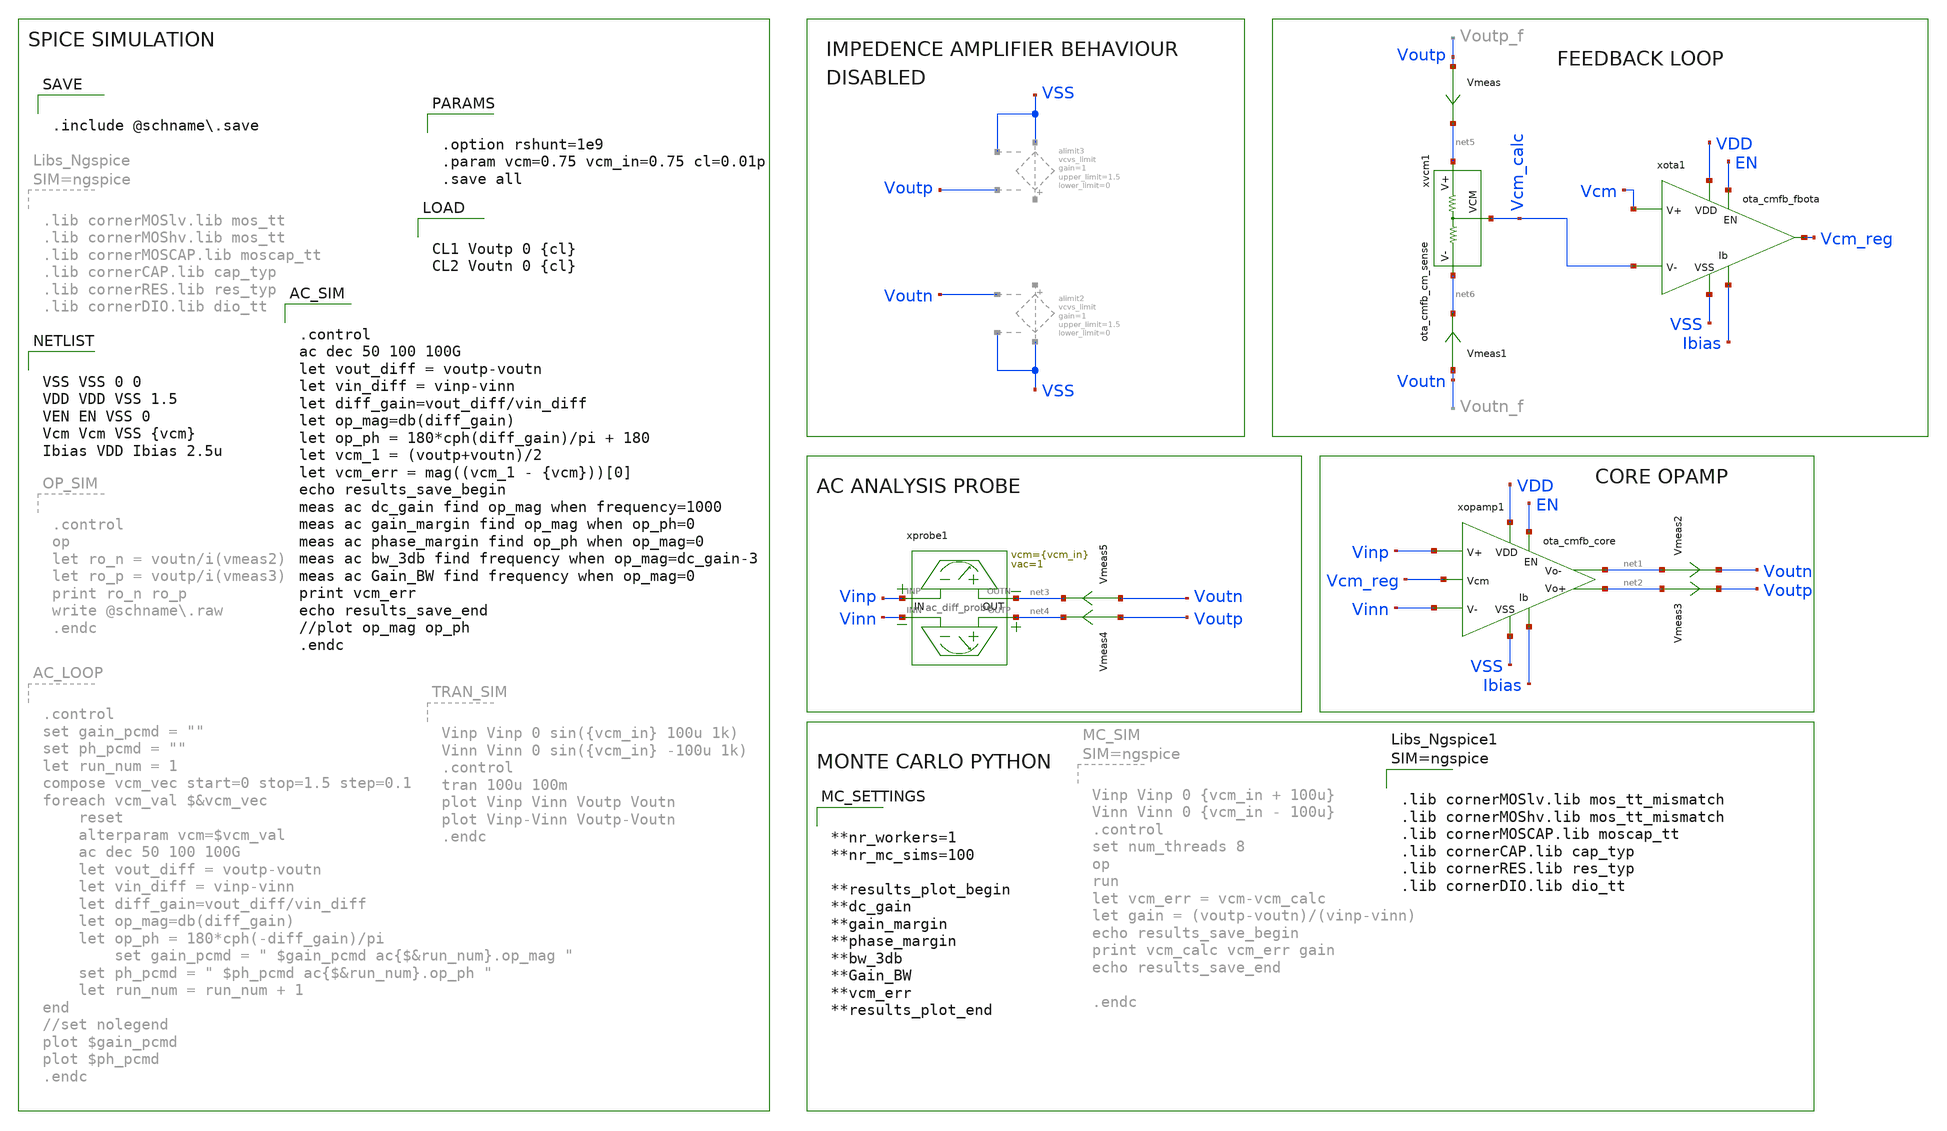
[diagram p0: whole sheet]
** sch_path: schema/ota_cmfb/ota_cmfb_tb.sch
**.subckt ota_cmfb_tb
xopamp1 VDD Vcm_reg Vinn Vinp Ibias net1 net2 VSS EN ota_cmfb_core
xprobe1 Vinp net3 Vinn net4 ac_diff_probe vcm={vcm_in} vac=1
xvcm1 net5 net6 Vcm_calc ota_cmfb_cm_sense
Vmeas Voutp net5 0
.save i(vmeas)
Vmeas1 Voutn net6 0
.save i(vmeas1)
xota1 VDD EN Ibias Vcm_calc Vcm Vcm_reg VSS ota_cmfb_fbota
Vmeas2 net1 Voutn 0
.save i(vmeas2)
Vmeas3 net2 Voutp 0
.save i(vmeas3)
Vmeas4 Voutp net4 0
.save i(vmeas4)
Vmeas5 Voutn net3 0
.save i(vmeas5)
**** begin user architecture code


VSS VSS 0 0
VDD VDD VSS 1.5
VEN EN VSS 0
Vcm Vcm VSS {vcm}
Ibias VDD Ibias 2.5u




.control
ac dec 50 100 100G
let vout_diff = voutp-voutn
let vin_diff = vinp-vinn
let diff_gain=vout_diff/vin_diff
let op_mag=db(diff_gain)
let op_ph = 180*cph(diff_gain)/pi + 180
let vcm_1 = (voutp+voutn)/2
let vcm_err = mag((vcm_1 - {vcm}))[0]
echo results_save_begin
meas ac dc_gain find op_mag when frequency=1000
meas ac gain_margin find op_mag when op_ph=0
meas ac phase_margin find op_ph when op_mag=0
meas ac bw_3db find frequency when op_mag=dc_gain-3
meas ac Gain_BW find frequency when op_mag=0
print vcm_err
echo results_save_end
//plot op_mag op_ph
.endc




.option rshunt=1e9
.param vcm=0.75 vcm_in=0.75 cl=0.01p
.save all




CL1 Voutp 0 {cl}
CL2 Voutn 0 {cl}



.include @schname.save



**nr_workers=1
**nr_mc_sims=100

**results_plot_begin
**dc_gain
**gain_margin
**phase_margin
**bw_3db
**Gain_BW
**vcm_err
**results_plot_end





.lib cornerMOSlv.lib mos_tt_mismatch
.lib cornerMOShv.lib mos_tt_mismatch
.lib cornerMOSCAP.lib moscap_tt
.lib cornerCAP.lib cap_typ
.lib cornerRES.lib res_typ
.lib cornerDIO.lib dio_tt



**** end user architecture code
**.ends

* expanding   symbol:  /foss/designs/Chipalooza2/schema/ota_cmfb_core/ota_cmfb_core.sym # of pins=9
** sym_path: schema/ota_cmfb_core/ota_cmfb_core.sym
** sch_path: schema/ota_cmfb_core/ota_cmfb_core.sch
.subckt ota_cmfb_core VDD Vcm_reg Vinn Vinp Ibias Voutn Voutp VSS EN
*.opin Voutn
*.opin Voutp
*.iopin VDD
*.iopin VSS
*.ipin Vinp
*.ipin Ibias
*.ipin Vinn
*.ipin Vcm_reg
*.ipin EN
XM1 Voutp_st1 Ibias VSS VSS sg13_lv_nmos w=0.5u l=10u ng=1 m=4 mm_ok=1
XM2 net1 Vinn Voutp_st1 VDD sg13_lv_pmos w=2.5u l=2u ng=1 m=8 mm_ok=1
XM3 Voutn_st1 Ibias VSS VSS sg13_lv_nmos w=0.5u l=10u ng=1 m=4 mm_ok=1
XM4 net1 Vinp Voutn_st1 VDD sg13_lv_pmos w=2.5u l=2u ng=1 m=8 mm_ok=1
XM5 VDD Vcm_reg net1 VDD sg13_lv_pmos w=5u l=10u ng=1 m=4 mm_ok=1
XM6 Ibias Ibias VSS VSS sg13_lv_nmos w=0.5u l=10u ng=1 m=1 mm_ok=1
XM7 Ibias EN VSS VSS sg13_lv_nmos w=0.15u l=0.13u ng=1 m=1 mm_ok=1
xsf1 VDD net2 Voutp Ibias VSS ota_cmfb_core_push_pull_output_stage
xsf2 VDD net3 Voutn Ibias VSS ota_cmfb_core_push_pull_output_stage
Vmeas Voutn_st1 net2 0
.save i(vmeas)
Vmeas1 Voutp_st1 net3 0
.save i(vmeas1)
.ends


* expanding   symbol:  /foss/designs/Chipalooza2/schema/ac_diff_probe/ac_diff_probe.sym # of pins=4
** sym_path: schema/ac_diff_probe/ac_diff_probe.sym
** sch_path: schema/ac_diff_probe/ac_diff_probe.sch
.subckt ac_diff_probe INP OUTN INN OUTP  vcm=0.75 vac=0.1
*.iopin OUTN
*.iopin INP
*.iopin OUTP
*.iopin INN
xprobe1 OUTN INP ac_probe vcm={vcm} vac={vac}
xprobe2 OUTP INN ac_probe vcm={vcm} vac=-{vac}
.ends


* expanding   symbol:  /foss/designs/Chipalooza2/schema/ota_cmfb_cm_sense/ota_cmfb_cm_sense.sym # of
*+ pins=3
** sym_path: schema/ota_cmfb_cm_sense/ota_cmfb_cm_sense.sym
** sch_path: schema/ota_cmfb_cm_sense/ota_cmfb_cm_sense.sch
.subckt ota_cmfb_cm_sense Voutp Voutn VCM
*.ipin Voutp
*.ipin Voutn
*.opin VCM
XR1 Voutn VCM 0 rhigh w=0.5e-6 l=1e-6*10 m=1 b=0 mm_ok=1
XR2 Voutp VCM 0 rhigh w=0.5e-6 l=1e-6*10 m=1 b=0 mm_ok=1
.ends


* expanding   symbol:  /foss/designs/Chipalooza2/schema/ota_cmfb_fbota/ota_cmfb_fbota.sym # of
*+ pins=7
** sym_path: schema/ota_cmfb_fbota/ota_cmfb_fbota.sym
** sch_path: schema/ota_cmfb_fbota/ota_cmfb_fbota.sch
.subckt ota_cmfb_fbota VDD EN Ibias Vinn Vinp Vout VSS
*.opin Vout
*.iopin VDD
*.iopin VSS
*.ipin Vinp
*.ipin Ibias
*.ipin Vinn
*.ipin EN
XMJ Vout mirror VSS VSS sg13_lv_nmos w=0.25u l=10u ng=1 m=4 mm_ok=1
XML Vout Vinn src_kl VDD sg13_lv_pmos w=2.5u l=2u ng=1 m=2 mm_ok=1
XMI mirror mirror VSS VSS sg13_lv_nmos w=0.25u l=10u ng=1 m=4 mm_ok=1
XMK mirror Vinp src_kl VDD sg13_lv_pmos w=2.5u l=2u ng=1 m=2 mm_ok=1
XMO src_kl tail_bias VDD VDD sg13_lv_pmos w=1.25u l=5u ng=1 m=8 mm_ok=1
XMN VDD tail_bias tail_bias VDD sg13_lv_pmos w=1.25u l=5u ng=1 m=2 mm_ok=1
XMH tail_bias Ibias VSS VSS sg13_lv_nmos w=0.25u l=10u ng=1 m=2 mm_ok=1
XMN1 mirror EN_N VSS VSS sg13_lv_nmos w=740.00n l=130.00n ng=1 m=1 mm_ok=1
XM2 VSS VSS tail_bias VSS sg13_lv_nmos w=0.25u l=0.5u ng=1 m=2 mm_ok=1
XMK1 mirror VDD VDD VDD sg13_lv_pmos w=2.5u l=0.5u ng=1 m=1 mm_ok=1
XMK2 Vout VDD VDD VDD sg13_lv_pmos w=2.5u l=0.5u ng=1 m=1 mm_ok=1
XMK3 src_kl VDD VDD VDD sg13_lv_pmos w=2.5u l=0.5u ng=1 m=2 mm_ok=1
XMK4 tail_bias VDD VDD VDD sg13_lv_pmos w=1.25u l=0.5u ng=1 m=2 mm_ok=1
XMN0 EN_N EN VSS VSS sg13_lv_nmos w=2.96u l=130.00n ng=1 m=1 mm_ok=1
XMP0 EN_N EN VDD VDD sg13_lv_pmos w=4.48u l=130.00n ng=1 m=1 mm_ok=1
.ends


* expanding   symbol:
*+  /foss/designs/Chipalooza2/schema/ota_cmfb_core/ota_cmfb_core_push_pull_output_stage.sym # of pins=5
** sym_path: schema/ota_cmfb_core/ota_cmfb_core_push_pull_output_stage.sym
** sch_path: schema/ota_cmfb_core/ota_cmfb_core_push_pull_output_stage.sch
.subckt ota_cmfb_core_push_pull_output_stage VDD Vin Vout Vbias VSS
*.iopin VSS
*.iopin VDD
*.ipin Vbias
*.ipin Vin
*.opin Vout
XM1 Vout Vin_shifted VSS VSS sg13_lv_nmos w=2.5u l=0.5u ng=1 m=1 mm_ok=1
XM2 VDD Vin Vout VDD sg13_lv_pmos w=5u l=0.5u ng=1 m=1 mm_ok=1
XM5 VDD Vbiasp net2 VDD sg13_lv_pmos w=10u l=3u ng=1 m=1 mm_ok=1
XM6 net1 Vbiasn VSS VSS sg13_lv_nmos w=5u l=0.5u ng=1 m=1 mm_ok=1
XM4 Vin_shifted Vcasp2 Vin VDD sg13_lv_pmos w=5u l=3u ng=1 m=1 mm_ok=1
XM15 Vin_shifted Vcasn net1 VSS sg13_lv_nmos w=5u l=0.5u ng=1 m=1 mm_ok=1
XM16 net2 Vcasp Vin VDD sg13_lv_pmos w=10u l=3u ng=1 m=1 mm_ok=1
XM3 Vin Vcasn2 Vin_shifted VSS sg13_lv_nmos w=1.4u l=3u ng=1 m=1 mm_ok=1
XM8 VDD Vbiasp Vbiasp VDD sg13_lv_pmos w=10u l=3u ng=1 m=1 mm_ok=1
XM9 Vbiasp Vcasp Vcasp VDD sg13_lv_pmos w=10u l=3u ng=1 m=1 mm_ok=1
XM13 Vcasp Vcasp2 Vcasp2 VDD sg13_lv_pmos w=5u l=3u ng=1 m=2 mm_ok=1
XM10 VDD Vbiasp Vcasn2 VDD sg13_lv_pmos w=10u l=3u ng=1 m=1 mm_ok=1
XM11 Vcasn2 Vcasn2 Vcasn VSS sg13_lv_nmos w=1.4u l=3u ng=1 m=2 mm_ok=1
XM12 Vcasn Vcasn Vbiasn VSS sg13_lv_nmos w=5u l=0.5u ng=1 m=1 mm_ok=1
XM14 Vbiasn Vbiasn VSS VSS sg13_lv_nmos w=5u l=0.5u ng=1 m=1 mm_ok=1
XM7 Vcasp2 Vbias VSS VSS sg13_lv_nmos w=2u l=1u ng=1 m=2 mm_ok=1
XR1 net3 Vout sub! rhigh w=0.5e-6 l=1e-6 m=1 b=0 mm_ok=1
XR2 net4 Vout sub! rhigh w=0.5e-6 l=1e-6*2 m=1 b=0 mm_ok=1
XC1 net3 Vin sg13_moscap_p w=5.0u l=5.0u m=3 mm_ok=1
XC2 net4 Vin_shifted sg13_moscap_p w=5.0u l=5.0u m=3 mm_ok=1
.ends


* expanding   symbol:  ac_probe/ac_probe.sym # of pins=2
** sym_path: schema/ac_probe/ac_probe.sym
** sch_path: schema/ac_probe/ac_probe.sch
.subckt ac_probe OUT IN  vcm=0.75 vac=0.01

*.iopin IN
*.iopin OUT
C1 0 IN 1 m=1
V1 IN 0 {vcm} ac {vac}
R1 OUT IN 1G m=1
.ends

.end
